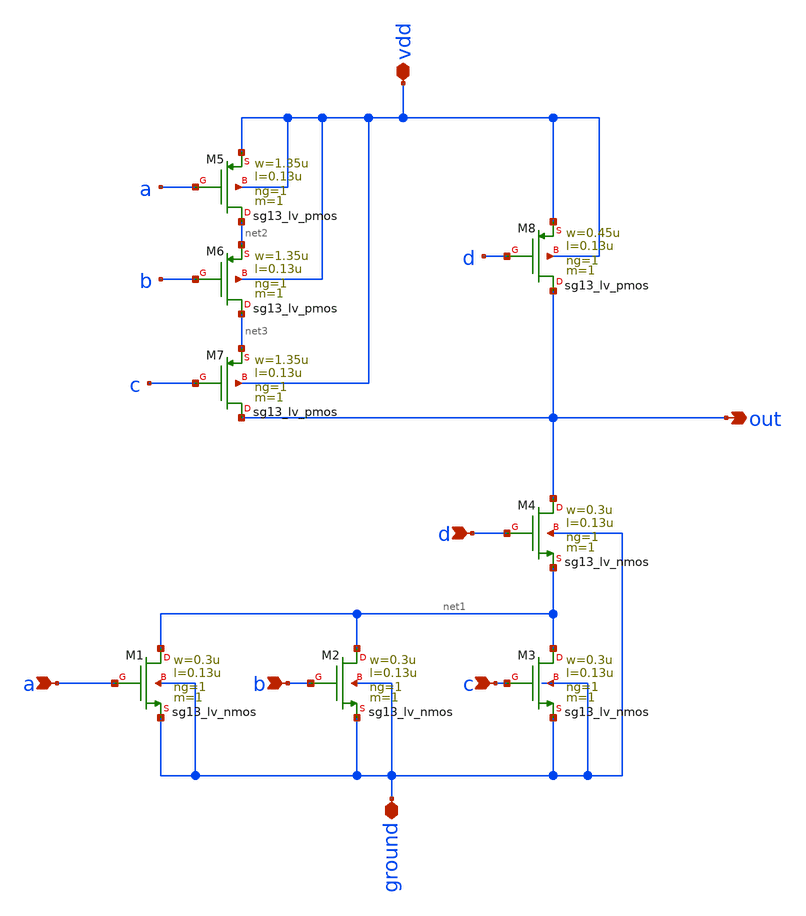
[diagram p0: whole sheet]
** sch_path: projekat/slucaj_3/schematic/funkcija.sch
**.subckt funkcija a b c d vdd ground out
*.ipin a
*.ipin b
*.ipin c
*.ipin d
*.iopin vdd
*.iopin ground
*.opin out
XM1 net1 a ground ground sg13_lv_nmos w=0.3u l=0.13u ng=1 m=1 mm_ok=1
XM2 net1 b ground ground sg13_lv_nmos w=0.3u l=0.13u ng=1 m=1 mm_ok=1
XM3 net1 c ground ground sg13_lv_nmos w=0.3u l=0.13u ng=1 m=1 mm_ok=1
XM4 out d net1 ground sg13_lv_nmos w=0.3u l=0.13u ng=1 m=1 mm_ok=1
XM5 net2 a vdd vdd sg13_lv_pmos w=1.35u l=0.13u ng=1 m=1 mm_ok=1
XM6 net3 b net2 vdd sg13_lv_pmos w=1.35u l=0.13u ng=1 m=1 mm_ok=1
XM7 out c net3 vdd sg13_lv_pmos w=1.35u l=0.13u ng=1 m=1 mm_ok=1
XM8 out d vdd vdd sg13_lv_pmos w=0.45u l=0.13u ng=1 m=1 mm_ok=1
**.ends
.end
